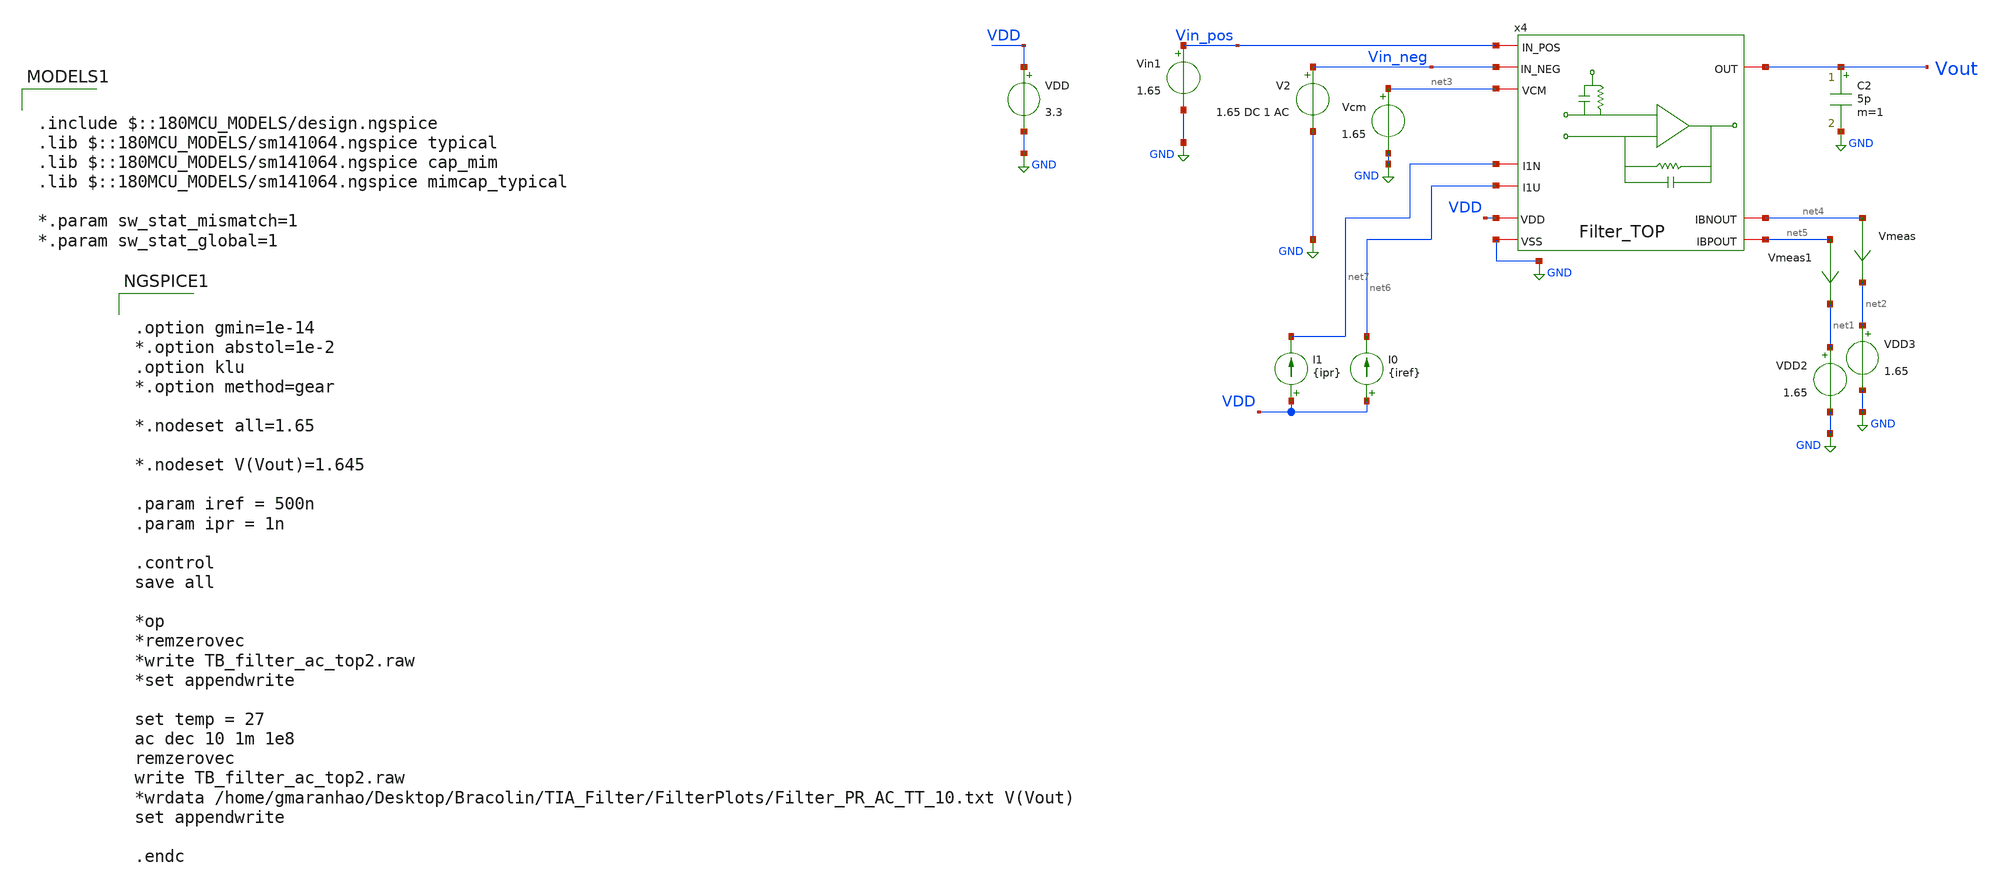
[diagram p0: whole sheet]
** sch_path: TIA_Filter/TB_filter_ac_top2.sch
**.subckt TB_filter_ac_top2
VDD VDD GND 3.3
C2 Vout GND 5p m=1
Vin1 Vin_pos GND 1.65
V2 Vin_neg GND 1.65 DC 1 AC
I0 VDD net6 {iref}
I1 VDD net7 {ipr}
Vmeas net4 net2 0
.save i(vmeas)
Vmeas1 net5 net1 0
.save i(vmeas1)
Vcm net3 GND 1.65
VDD2 net1 GND 1.65
VDD3 net2 GND 1.65
x4 Vin_pos Vin_neg net3 Vout VDD GND net7 net6 net4 net5 Filter_TOP
**** begin user architecture code

.include $::180MCU_MODELS/design.ngspice
.lib $::180MCU_MODELS/sm141064.ngspice typical
.lib $::180MCU_MODELS/sm141064.ngspice cap_mim
.lib $::180MCU_MODELS/sm141064.ngspice mimcap_typical

*.param sw_stat_mismatch=1
*.param sw_stat_global=1



.option gmin=1e-14
*.option abstol=1e-2
.option klu
*.option method=gear

*.nodeset all=1.65

*.nodeset V(Vout)=1.645

.param iref = 500n
.param ipr = 1n

.control
save all

*op
*remzerovec
*write TB_filter_ac_top2.raw
*set appendwrite

set temp = 27
ac dec 10 1m 1e8
remzerovec
write TB_filter_ac_top2.raw
*wrdata /home/gmaranhao/Desktop/Bracolin/TIA_Filter/FilterPlots/Filter_PR_AC_TT_10.txt V(Vout)
set appendwrite

.endc


**** end user architecture code
**.ends
.GLOBAL GND
.end
